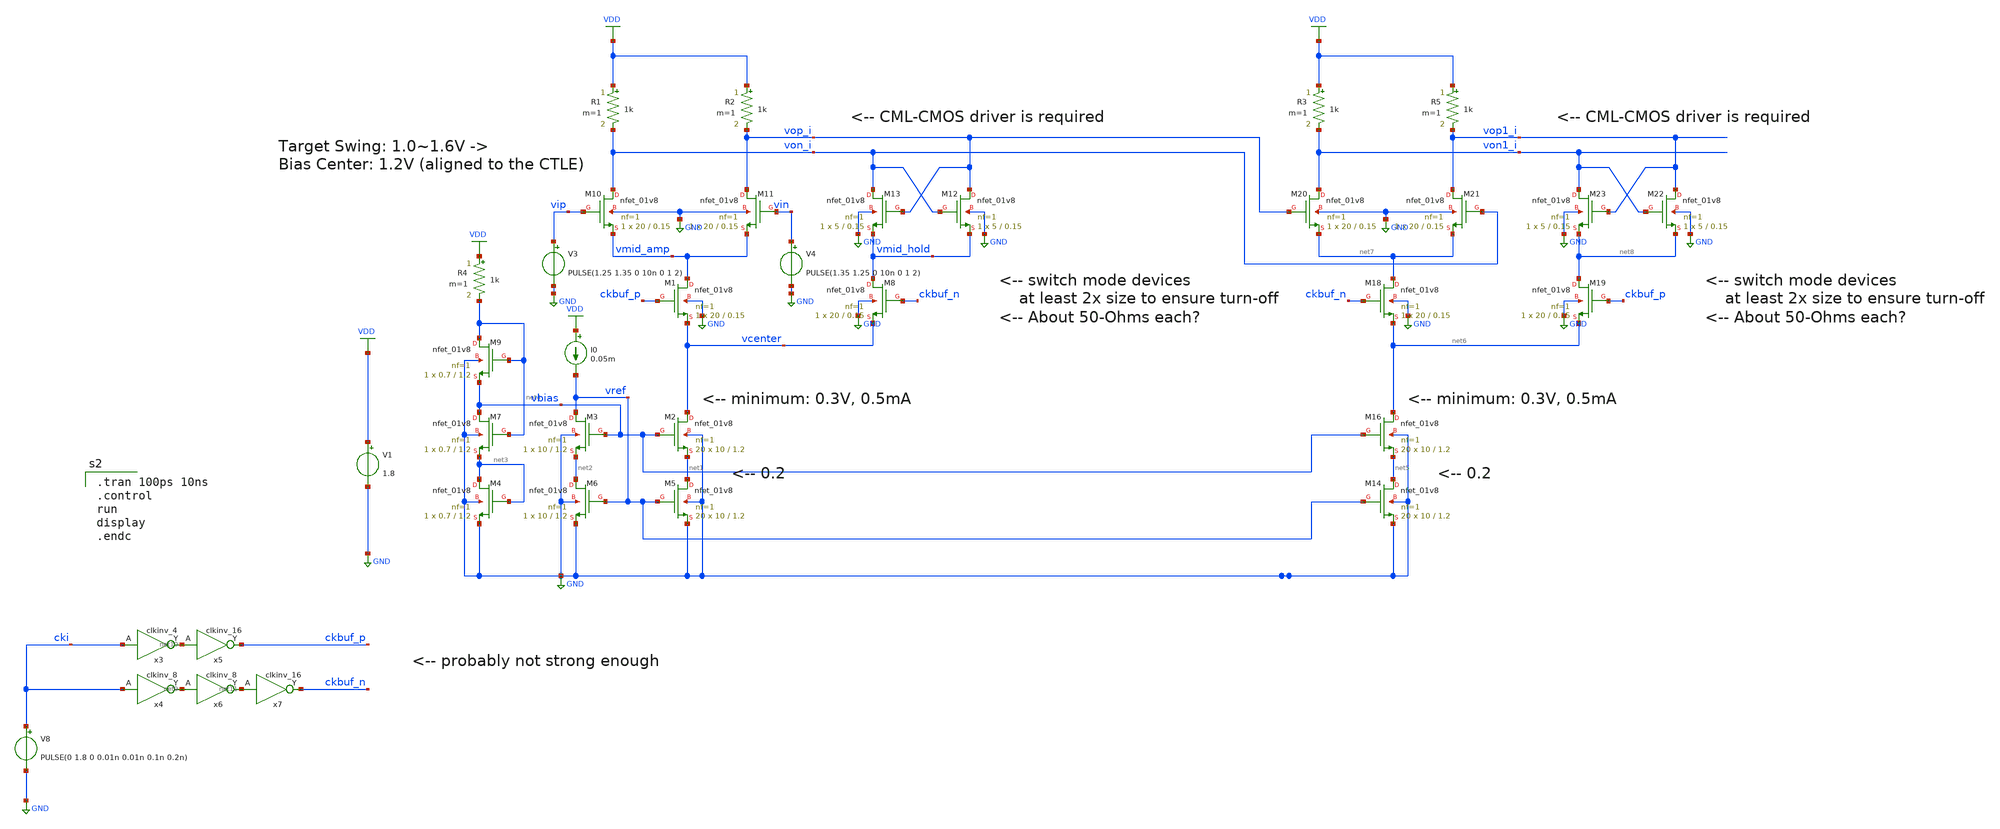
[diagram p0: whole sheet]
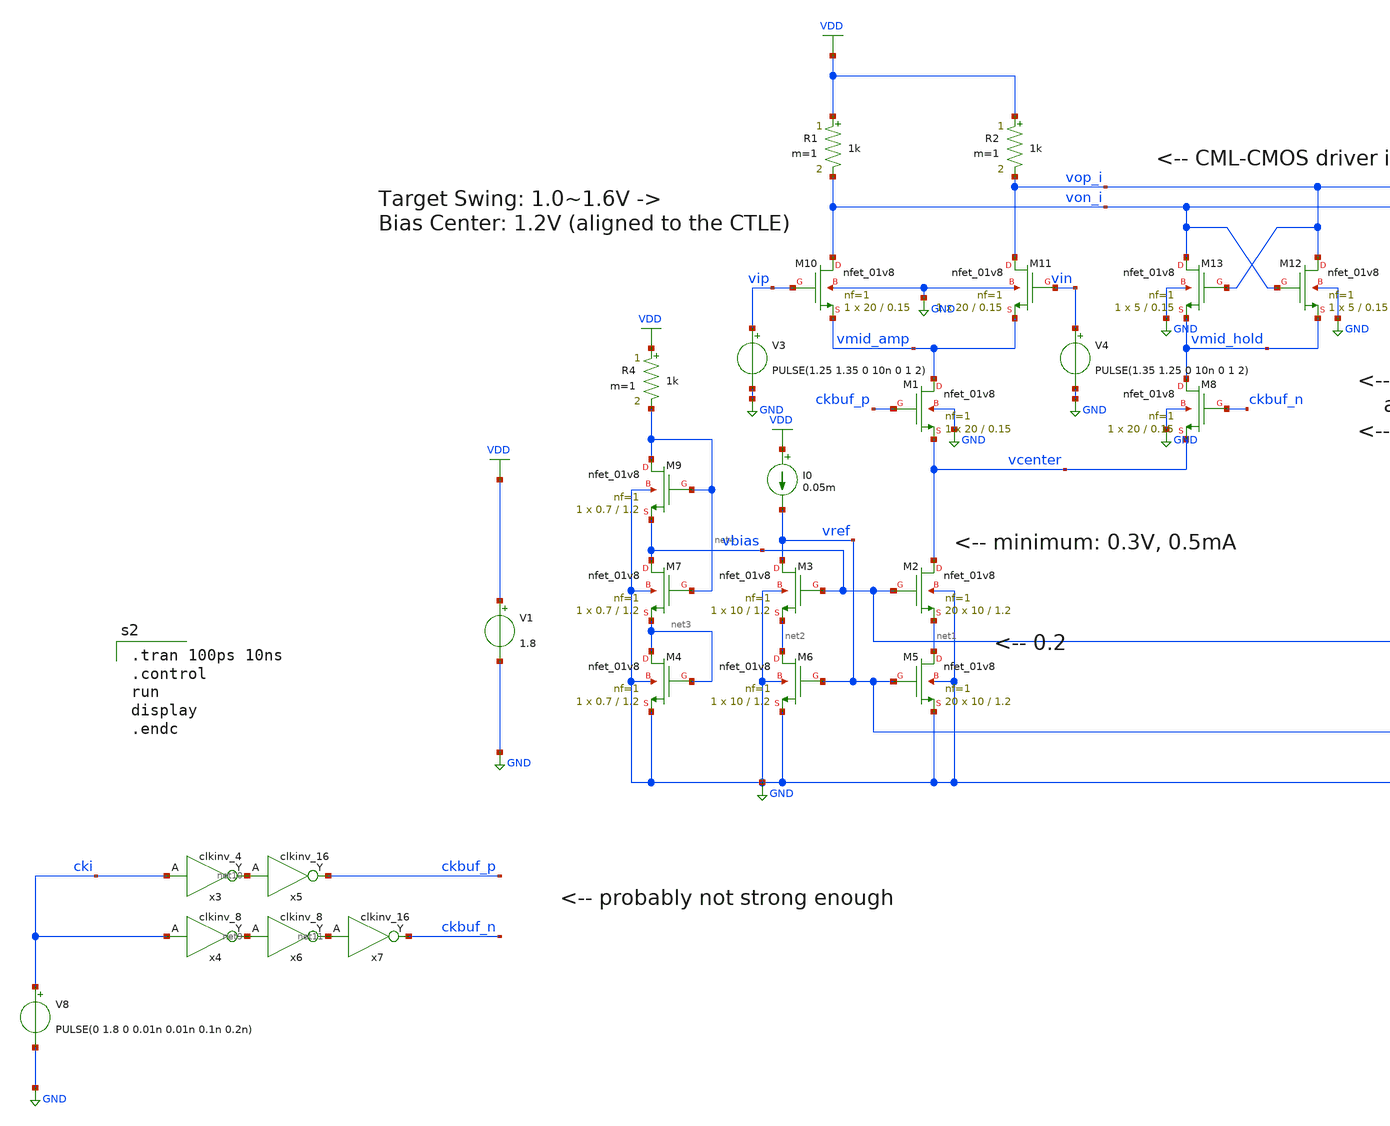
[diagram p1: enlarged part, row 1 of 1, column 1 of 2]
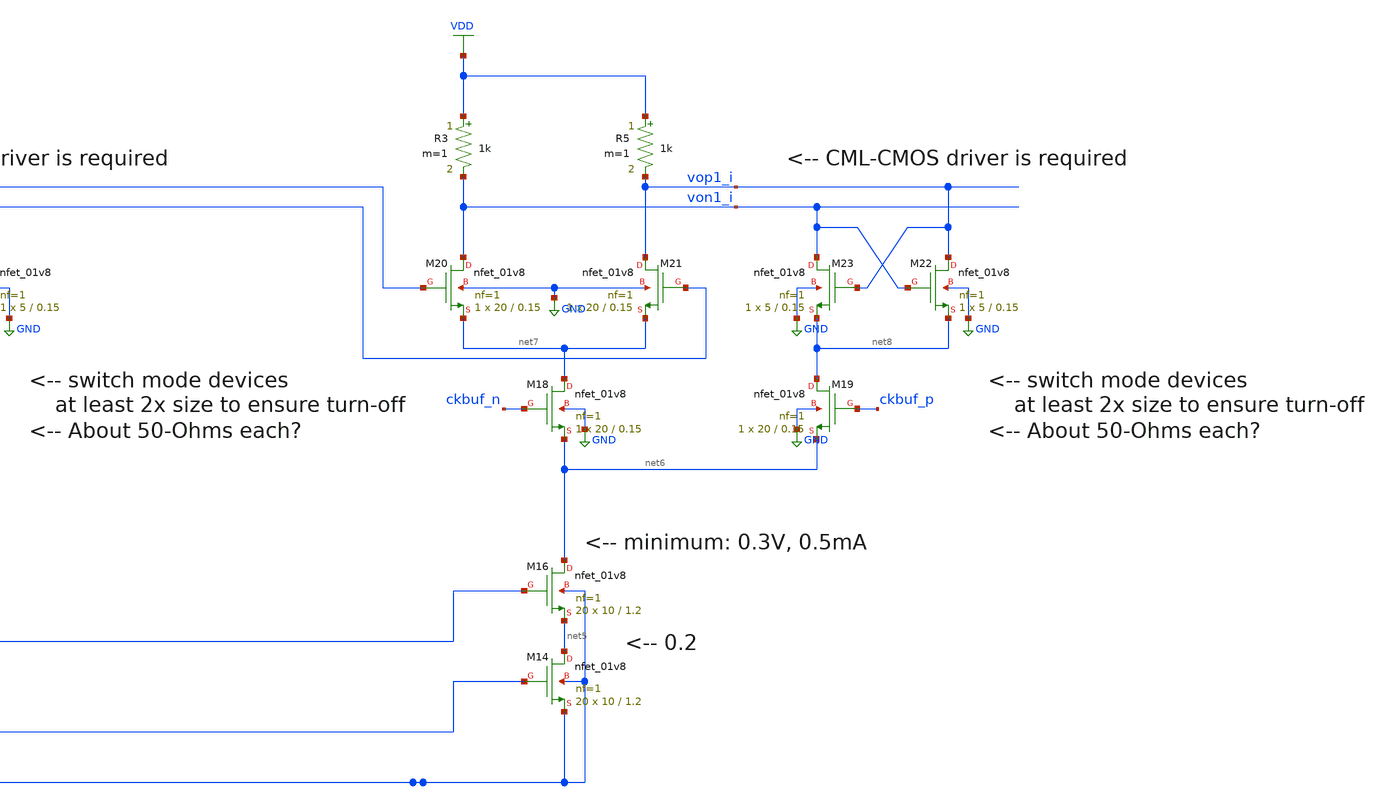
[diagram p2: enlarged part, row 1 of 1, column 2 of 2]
** sch_path: xschem/CML_latch_1mA_transient_tb.sch
**.subckt CML_latch_1mA_transient_tb
V1 VDD GND 1.8
XM5 net1 vref GND GND sky130_fd_pr__nfet_01v8 L=1.2 W=10 nf=1 ad='int((nf+1)/2) * W/nf * 0.29' as='int((nf+2)/2) * W/nf * 0.29'
+ pd='2*int((nf+1)/2) * (W/nf + 0.29)' ps='2*int((nf+2)/2) * (W/nf + 0.29)' nrd='0.29 / W' nrs='0.29 / W'
+ sa=0 sb=0 sd=0 mult=20 m=20
XM6 net2 vref GND GND sky130_fd_pr__nfet_01v8 L=1.2 W=10 nf=1 ad='int((nf+1)/2) * W/nf * 0.29' as='int((nf+2)/2) * W/nf * 0.29'
+ pd='2*int((nf+1)/2) * (W/nf + 0.29)' ps='2*int((nf+2)/2) * (W/nf + 0.29)' nrd='0.29 / W' nrs='0.29 / W'
+ sa=0 sb=0 sd=0 mult=1 m=1
I0 VDD vref 0.05m
XM2 vcenter vbias net1 GND sky130_fd_pr__nfet_01v8 L=1.2 W=10 nf=1 ad='int((nf+1)/2) * W/nf * 0.29' as='int((nf+2)/2) * W/nf * 0.29'
+ pd='2*int((nf+1)/2) * (W/nf + 0.29)' ps='2*int((nf+2)/2) * (W/nf + 0.29)' nrd='0.29 / W' nrs='0.29 / W'
+ sa=0 sb=0 sd=0 mult=20 m=20
XM3 vref vbias net2 GND sky130_fd_pr__nfet_01v8 L=1.2 W=10 nf=1 ad='int((nf+1)/2) * W/nf * 0.29' as='int((nf+2)/2) * W/nf * 0.29'
+ pd='2*int((nf+1)/2) * (W/nf + 0.29)' ps='2*int((nf+2)/2) * (W/nf + 0.29)' nrd='0.29 / W' nrs='0.29 / W'
+ sa=0 sb=0 sd=0 mult=1 m=1
XM4 net3 net3 GND GND sky130_fd_pr__nfet_01v8 L=1.2 W=0.7 nf=1 ad='int((nf+1)/2) * W/nf * 0.29' as='int((nf+2)/2) * W/nf * 0.29'
+ pd='2*int((nf+1)/2) * (W/nf + 0.29)' ps='2*int((nf+2)/2) * (W/nf + 0.29)' nrd='0.29 / W' nrs='0.29 / W'
+ sa=0 sb=0 sd=0 mult=1 m=1
XM7 vbias net4 net3 GND sky130_fd_pr__nfet_01v8 L=1.2 W=0.7 nf=1 ad='int((nf+1)/2) * W/nf * 0.29' as='int((nf+2)/2) * W/nf * 0.29'
+ pd='2*int((nf+1)/2) * (W/nf + 0.29)' ps='2*int((nf+2)/2) * (W/nf + 0.29)' nrd='0.29 / W' nrs='0.29 / W'
+ sa=0 sb=0 sd=0 mult=1 m=1
XM9 net4 net4 vbias GND sky130_fd_pr__nfet_01v8 L=1.2 W=0.7 nf=1 ad='int((nf+1)/2) * W/nf * 0.29' as='int((nf+2)/2) * W/nf * 0.29'
+ pd='2*int((nf+1)/2) * (W/nf + 0.29)' ps='2*int((nf+2)/2) * (W/nf + 0.29)' nrd='0.29 / W' nrs='0.29 / W'
+ sa=0 sb=0 sd=0 mult=1 m=1
R4 VDD net4 1k m=1
XM1 vmid_amp ckbuf_p vcenter GND sky130_fd_pr__nfet_01v8 L=0.15 W=20 nf=1 ad='int((nf+1)/2) * W/nf * 0.29'
+ as='int((nf+2)/2) * W/nf * 0.29' pd='2*int((nf+1)/2) * (W/nf + 0.29)' ps='2*int((nf+2)/2) * (W/nf + 0.29)'
+ nrd='0.29 / W' nrs='0.29 / W' sa=0 sb=0 sd=0 mult=1 m=1
XM8 vmid_hold ckbuf_n vcenter GND sky130_fd_pr__nfet_01v8 L=0.15 W=20 nf=1 ad='int((nf+1)/2) * W/nf * 0.29'
+ as='int((nf+2)/2) * W/nf * 0.29' pd='2*int((nf+1)/2) * (W/nf + 0.29)' ps='2*int((nf+2)/2) * (W/nf + 0.29)'
+ nrd='0.29 / W' nrs='0.29 / W' sa=0 sb=0 sd=0 mult=1 m=1
XM10 von_i vip vmid_amp GND sky130_fd_pr__nfet_01v8 L=0.15 W=20 nf=1 ad='int((nf+1)/2) * W/nf * 0.29'
+ as='int((nf+2)/2) * W/nf * 0.29' pd='2*int((nf+1)/2) * (W/nf + 0.29)' ps='2*int((nf+2)/2) * (W/nf + 0.29)'
+ nrd='0.29 / W' nrs='0.29 / W' sa=0 sb=0 sd=0 mult=1 m=1
XM11 vop_i vin vmid_amp GND sky130_fd_pr__nfet_01v8 L=0.15 W=20 nf=1 ad='int((nf+1)/2) * W/nf * 0.29'
+ as='int((nf+2)/2) * W/nf * 0.29' pd='2*int((nf+1)/2) * (W/nf + 0.29)' ps='2*int((nf+2)/2) * (W/nf + 0.29)'
+ nrd='0.29 / W' nrs='0.29 / W' sa=0 sb=0 sd=0 mult=1 m=1
XM12 vop_i von_i vmid_hold GND sky130_fd_pr__nfet_01v8 L=0.15 W=5 nf=1 ad='int((nf+1)/2) * W/nf * 0.29'
+ as='int((nf+2)/2) * W/nf * 0.29' pd='2*int((nf+1)/2) * (W/nf + 0.29)' ps='2*int((nf+2)/2) * (W/nf + 0.29)'
+ nrd='0.29 / W' nrs='0.29 / W' sa=0 sb=0 sd=0 mult=1 m=1
XM13 von_i vop_i vmid_hold GND sky130_fd_pr__nfet_01v8 L=0.15 W=5 nf=1 ad='int((nf+1)/2) * W/nf * 0.29'
+ as='int((nf+2)/2) * W/nf * 0.29' pd='2*int((nf+1)/2) * (W/nf + 0.29)' ps='2*int((nf+2)/2) * (W/nf + 0.29)'
+ nrd='0.29 / W' nrs='0.29 / W' sa=0 sb=0 sd=0 mult=1 m=1
R1 VDD von_i 1k m=1
R2 VDD vop_i 1k m=1
V8 cki GND PULSE(0 1.8 0 0.01n 0.01n 0.1n 0.2n)
x4 cki gnd gnd vdd vdd net9 sky130_fd_sc_hs__clkinv_8
x3 cki gnd gnd vdd vdd net10 sky130_fd_sc_hs__clkinv_4
x5 net10 gnd gnd vdd vdd ckbuf_p sky130_fd_sc_hs__clkinv_16
x6 net9 gnd gnd vdd vdd net11 sky130_fd_sc_hs__clkinv_8
x7 net11 gnd gnd vdd vdd ckbuf_n sky130_fd_sc_hs__clkinv_16
V3 vip GND PULSE(1.25 1.35 0 10n 0 1 2)
V4 vin GND PULSE(1.35 1.25 0 10n 0 1 2)
XM14 net5 vref GND GND sky130_fd_pr__nfet_01v8 L=1.2 W=10 nf=1 ad='int((nf+1)/2) * W/nf * 0.29' as='int((nf+2)/2) * W/nf * 0.29'
+ pd='2*int((nf+1)/2) * (W/nf + 0.29)' ps='2*int((nf+2)/2) * (W/nf + 0.29)' nrd='0.29 / W' nrs='0.29 / W'
+ sa=0 sb=0 sd=0 mult=20 m=20
XM16 net6 vbias net5 GND sky130_fd_pr__nfet_01v8 L=1.2 W=10 nf=1 ad='int((nf+1)/2) * W/nf * 0.29' as='int((nf+2)/2) * W/nf * 0.29'
+ pd='2*int((nf+1)/2) * (W/nf + 0.29)' ps='2*int((nf+2)/2) * (W/nf + 0.29)' nrd='0.29 / W' nrs='0.29 / W'
+ sa=0 sb=0 sd=0 mult=20 m=20
XM18 net7 ckbuf_n net6 GND sky130_fd_pr__nfet_01v8 L=0.15 W=20 nf=1 ad='int((nf+1)/2) * W/nf * 0.29'
+ as='int((nf+2)/2) * W/nf * 0.29' pd='2*int((nf+1)/2) * (W/nf + 0.29)' ps='2*int((nf+2)/2) * (W/nf + 0.29)'
+ nrd='0.29 / W' nrs='0.29 / W' sa=0 sb=0 sd=0 mult=1 m=1
XM19 net8 ckbuf_p net6 GND sky130_fd_pr__nfet_01v8 L=0.15 W=20 nf=1 ad='int((nf+1)/2) * W/nf * 0.29'
+ as='int((nf+2)/2) * W/nf * 0.29' pd='2*int((nf+1)/2) * (W/nf + 0.29)' ps='2*int((nf+2)/2) * (W/nf + 0.29)'
+ nrd='0.29 / W' nrs='0.29 / W' sa=0 sb=0 sd=0 mult=1 m=1
XM20 von1_i vop_i net7 GND sky130_fd_pr__nfet_01v8 L=0.15 W=20 nf=1 ad='int((nf+1)/2) * W/nf * 0.29'
+ as='int((nf+2)/2) * W/nf * 0.29' pd='2*int((nf+1)/2) * (W/nf + 0.29)' ps='2*int((nf+2)/2) * (W/nf + 0.29)'
+ nrd='0.29 / W' nrs='0.29 / W' sa=0 sb=0 sd=0 mult=1 m=1
XM21 vop1_i von_i net7 GND sky130_fd_pr__nfet_01v8 L=0.15 W=20 nf=1 ad='int((nf+1)/2) * W/nf * 0.29'
+ as='int((nf+2)/2) * W/nf * 0.29' pd='2*int((nf+1)/2) * (W/nf + 0.29)' ps='2*int((nf+2)/2) * (W/nf + 0.29)'
+ nrd='0.29 / W' nrs='0.29 / W' sa=0 sb=0 sd=0 mult=1 m=1
XM22 vop1_i von1_i net8 GND sky130_fd_pr__nfet_01v8 L=0.15 W=5 nf=1 ad='int((nf+1)/2) * W/nf * 0.29'
+ as='int((nf+2)/2) * W/nf * 0.29' pd='2*int((nf+1)/2) * (W/nf + 0.29)' ps='2*int((nf+2)/2) * (W/nf + 0.29)'
+ nrd='0.29 / W' nrs='0.29 / W' sa=0 sb=0 sd=0 mult=1 m=1
XM23 von1_i vop1_i net8 GND sky130_fd_pr__nfet_01v8 L=0.15 W=5 nf=1 ad='int((nf+1)/2) * W/nf * 0.29'
+ as='int((nf+2)/2) * W/nf * 0.29' pd='2*int((nf+1)/2) * (W/nf + 0.29)' ps='2*int((nf+2)/2) * (W/nf + 0.29)'
+ nrd='0.29 / W' nrs='0.29 / W' sa=0 sb=0 sd=0 mult=1 m=1
R3 VDD von1_i 1k m=1
R5 VDD vop1_i 1k m=1
**** begin user architecture code
.lib $::SKYWATER_MODELS/sky130.lib.spice tt
.include $::PDKPATH/libs.ref/sky130_fd_sc_hs/spice/sky130_fd_sc_hs.spice


.tran 100ps 10ns
.control
run
display
.endc


**** end user architecture code
**.ends
.GLOBAL GND
.GLOBAL VDD
.end
